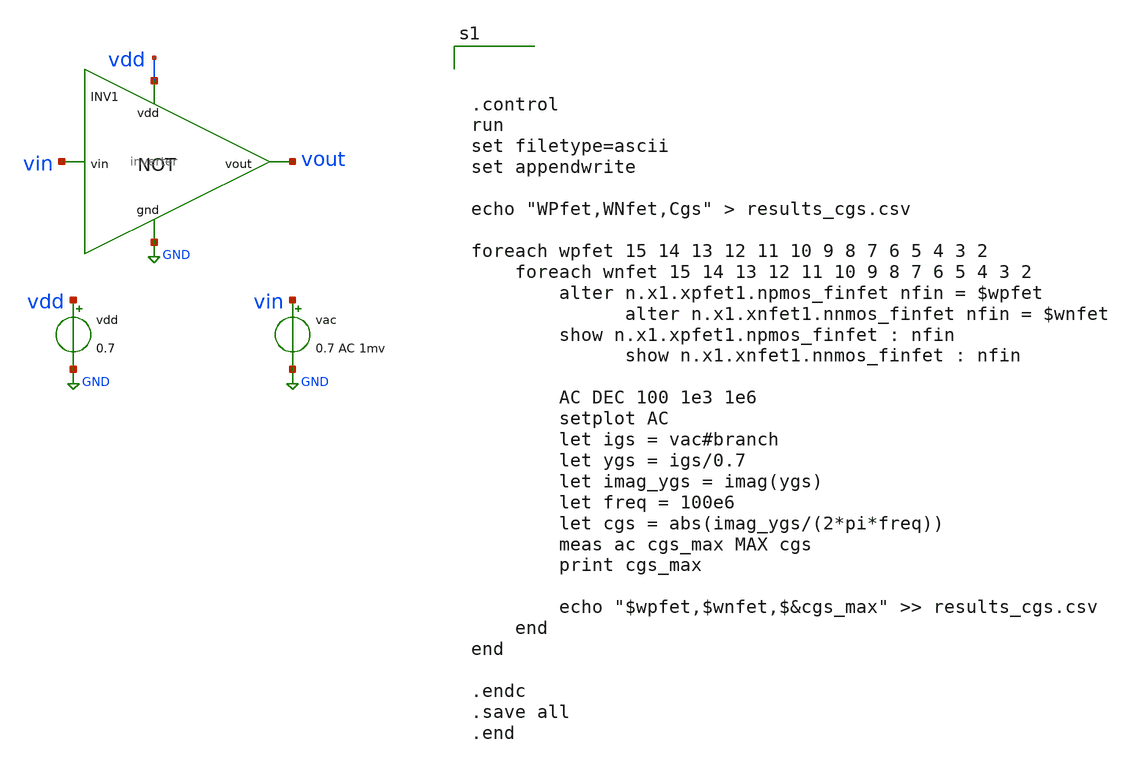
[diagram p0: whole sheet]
** sch_path: Xschem_ASAP7/inverter_ac.sch
**.subckt inverter_ac
x1 vdd vin vout GND inverter
vdd vdd GND 0.7
vac vin GND 0.7 AC 1mv
**** begin user architecture code



.control
run
set filetype=ascii
set appendwrite

echo "WPfet,WNfet,Cgs" > results_cgs.csv

foreach wpfet 15 14 13 12 11 10 9 8 7 6 5 4 3 2
	foreach wnfet 15 14 13 12 11 10 9 8 7 6 5 4 3 2
		alter n.x1.xpfet1.npmos_finfet nfin = $wpfet
      		alter n.x1.xnfet1.nnmos_finfet nfin = $wnfet
		show n.x1.xpfet1.npmos_finfet : nfin
      		show n.x1.xnfet1.nnmos_finfet : nfin

		AC DEC 100 1e3 1e6
		setplot AC
		let igs = vac#branch
		let ygs = igs/0.7
		let imag_ygs = imag(ygs)
		let freq = 100e6
		let cgs = abs(imag_ygs/(2*pi*freq))
		meas ac cgs_max MAX cgs
		print cgs_max

		echo "$wpfet,$wnfet,$&cgs_max" >> results_cgs.csv
	end
end

.endc
.save all
.end


**** end user architecture code
**.ends

* expanding   symbol:  inverter.sym # of pins=4
** sym_path: Xschem_ASAP7/inverter.sym
** sch_path: Xschem_ASAP7/inverter.sch
.subckt inverter vdd vin vout gnd
*.ipin vin
*.ipin vdd
*.ipin gnd
*.opin vout
Xnfet1 vout vin gnd gnd asap_7nm_nfet l=7e-009 nfin=13
Xpfet1 vout vin vdd vdd asap_7nm_pfet l=7e-009 nfin=14
.ends

.GLOBAL GND
.end
